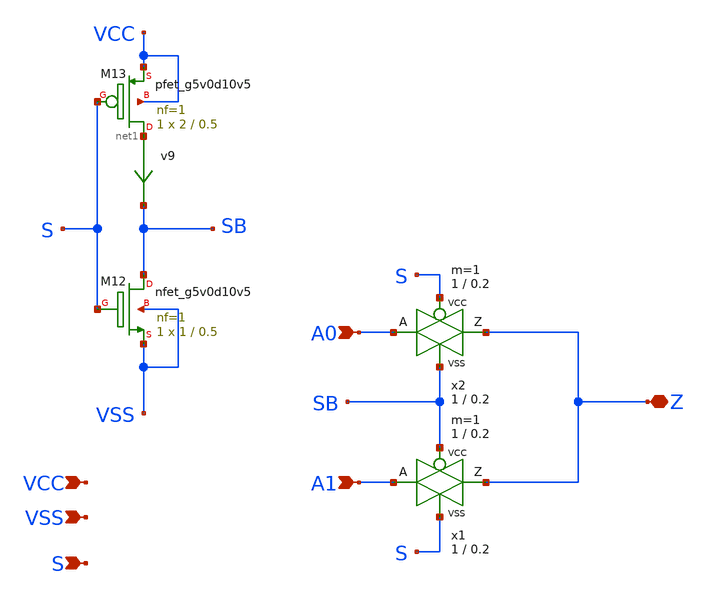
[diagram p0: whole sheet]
** sch_path: xschem/mux2to1.sch
**.subckt mux2to1 VCC VSS A0 A1 Z S
*.ipin VCC
*.ipin VSS
*.ipin A0
*.ipin A1
*.iopin Z
*.ipin S
x2 Z A0 S SB VCC VSS passgate_3p3 W_N=1 L_N=0.2 W_P=1 L_P=0.2 m=1
x1 Z A1 SB S VCC VSS passgate_3p3 W_N=1 L_N=0.2 W_P=1 L_P=0.2 m=1
XM12 SB S VSS VSS sky130_fd_pr__nfet_g5v0d10v5 L=0.5 W=1 nf=1 ad='int((nf+1)/2) * W/nf * 0.29' as='int((nf+2)/2) * W/nf * 0.29'
+ pd='2*int((nf+1)/2) * (W/nf + 0.29)' ps='2*int((nf+2)/2) * (W/nf + 0.29)' nrd='0.29 / W' nrs='0.29 / W'
+ sa=0 sb=0 sd=0 mult=1 m=1
v9 net1 SB 0
.save i(v9)
XM13 net1 S VCC VCC sky130_fd_pr__pfet_g5v0d10v5 L=0.5 W=2 nf=1 ad='int((nf+1)/2) * W/nf * 0.29' as='int((nf+2)/2) * W/nf * 0.29'
+ pd='2*int((nf+1)/2) * (W/nf + 0.29)' ps='2*int((nf+2)/2) * (W/nf + 0.29)' nrd='0.29 / W' nrs='0.29 / W'
+ sa=0 sb=0 sd=0 mult=1 m=1
**.ends
.end
